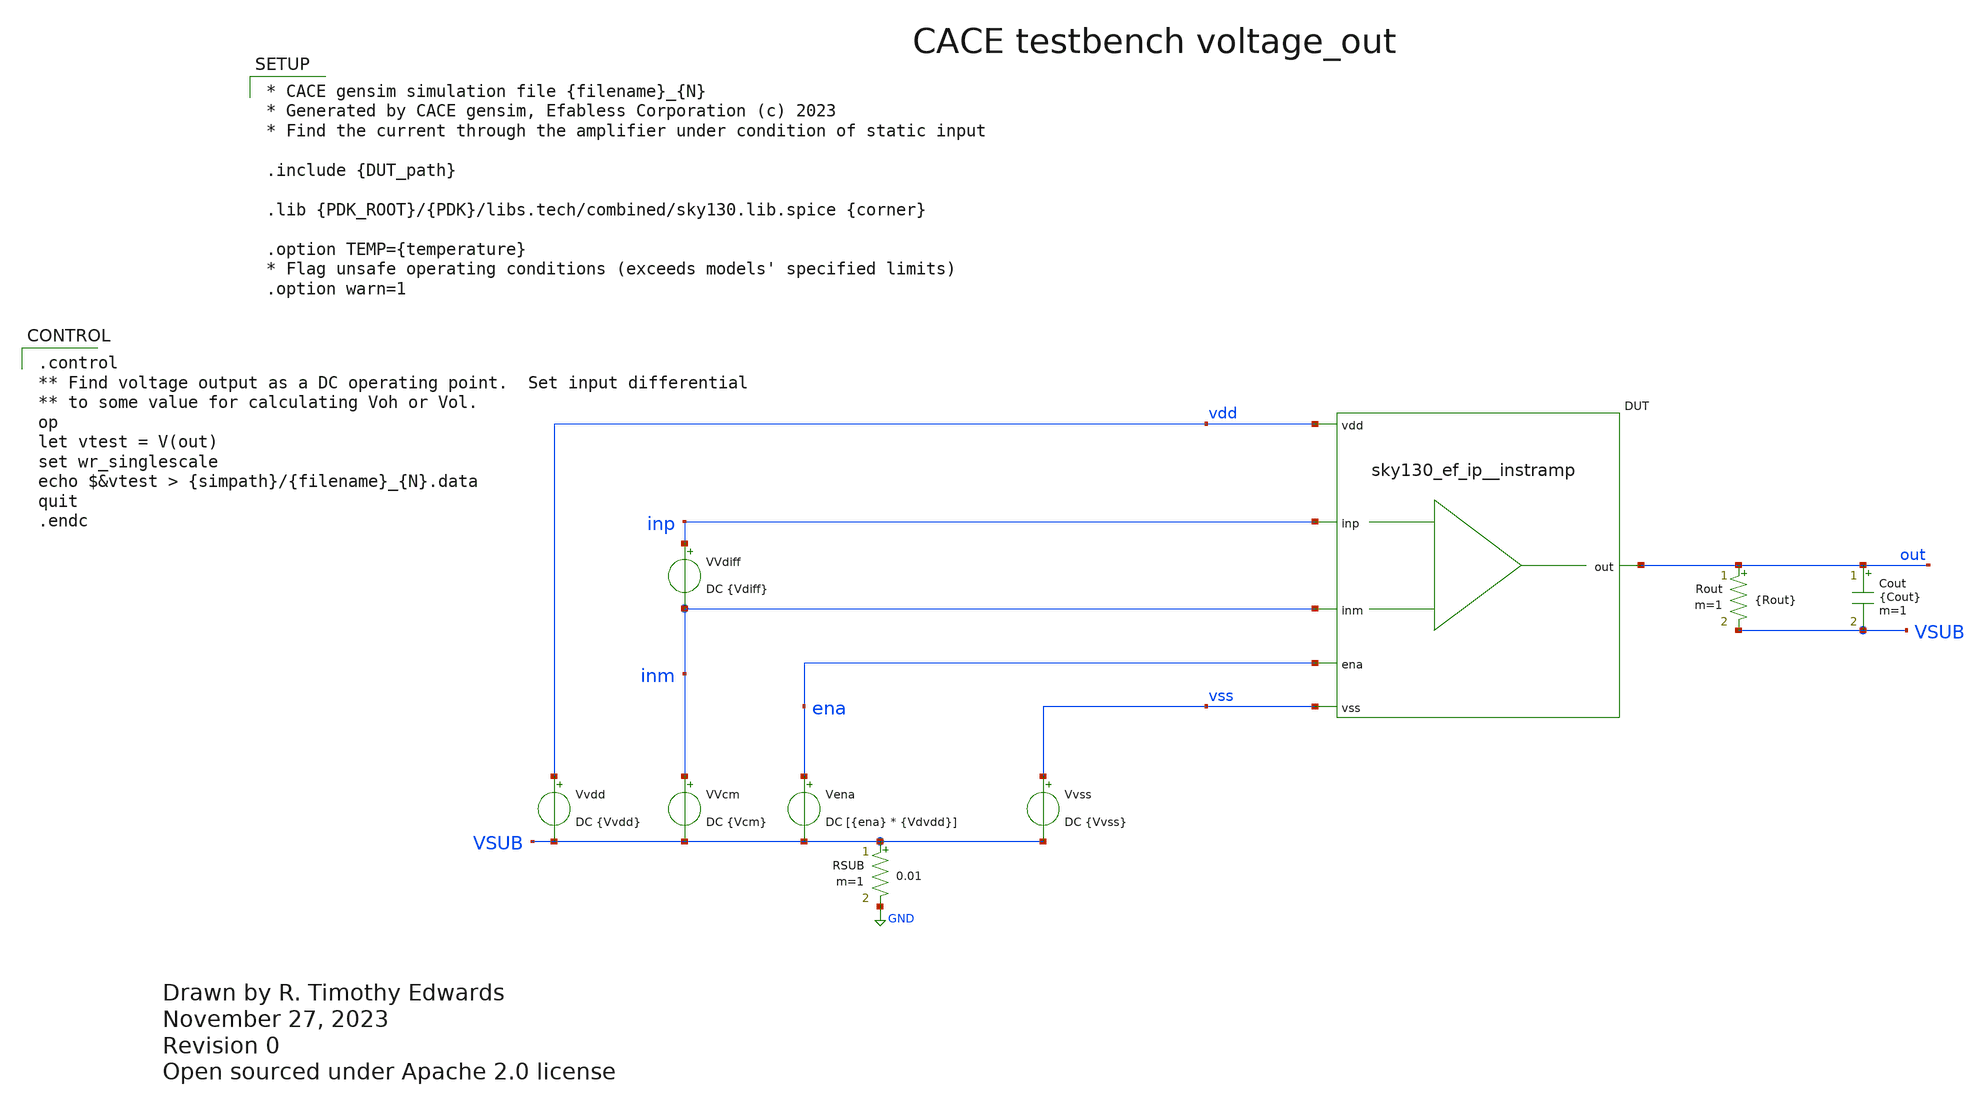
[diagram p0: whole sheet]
** sch_path: cace/voltage_out.sch
* Open sourced under Apache 2.0 license
**.subckt voltage_out
VVcm inm VSUB DC {Vcm}
Vena ena VSUB DC [{ena} * {Vdvdd}]
Vvss vss VSUB DC {Vvss}
Rout out VSUB {Rout} m=1
Cout out VSUB {Cout} m=1
Vvdd vdd VSUB DC {Vvdd}
RSUB VSUB GND 0.01 m=1
XDUT {PIN|vdd|vdd} {PIN|vss|vss} {PIN|inm|inm} {PIN|inp|inp} {PIN|out|out} {PIN|ena|ena} {DUT_name}
VVdiff inp inm DC {Vdiff}
**** begin user architecture code

.control
** Find voltage output as a DC operating point.  Set input differential
** to some value for calculating Voh or Vol.
op
let vtest = V(out)
set wr_singlescale
echo $&vtest > {simpath}/{filename}_{N}.data
quit
.endc



* CACE gensim simulation file {filename}_{N}
* Generated by CACE gensim, Efabless Corporation (c) 2023
* Find the current through the amplifier under condition of static input

.include {DUT_path}

.lib {PDK_ROOT}/{PDK}/libs.tech/combined/sky130.lib.spice {corner}

.option TEMP={temperature}
* Flag unsafe operating conditions (exceeds models' specified limits)
.option warn=1


**** end user architecture code
**.ends
.GLOBAL GND
.end
